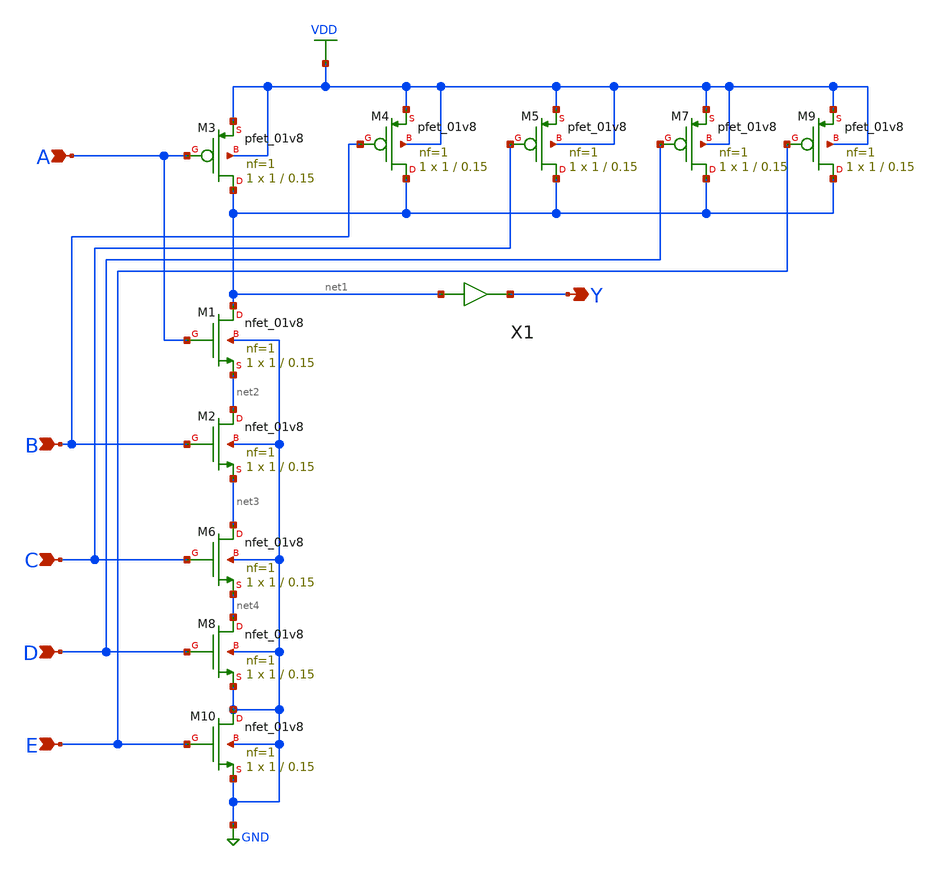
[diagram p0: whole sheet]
** sch_path: gates/AND5.sch
**.subckt AND5 A B Y C D E
*.ipin A
*.ipin B
*.opin Y
*.ipin C
*.ipin D
*.ipin E
XM1 net1 A net2 GND sky130_fd_pr__nfet_01v8 L=0.15 W=1 nf=1 ad='int((nf+1)/2) * W/nf * 0.29' as='int((nf+2)/2) * W/nf * 0.29'
+ pd='2*int((nf+1)/2) * (W/nf + 0.29)' ps='2*int((nf+2)/2) * (W/nf + 0.29)' nrd='0.29 / W' nrs='0.29 / W'
+ sa=0 sb=0 sd=0 mult=1 m=1
XM2 net2 B net3 GND sky130_fd_pr__nfet_01v8 L=0.15 W=1 nf=1 ad='int((nf+1)/2) * W/nf * 0.29' as='int((nf+2)/2) * W/nf * 0.29'
+ pd='2*int((nf+1)/2) * (W/nf + 0.29)' ps='2*int((nf+2)/2) * (W/nf + 0.29)' nrd='0.29 / W' nrs='0.29 / W'
+ sa=0 sb=0 sd=0 mult=1 m=1
XM3 net1 A VDD VDD sky130_fd_pr__pfet_01v8 L=0.15 W=1 nf=1 ad='int((nf+1)/2) * W/nf * 0.29' as='int((nf+2)/2) * W/nf * 0.29'
+ pd='2*int((nf+1)/2) * (W/nf + 0.29)' ps='2*int((nf+2)/2) * (W/nf + 0.29)' nrd='0.29 / W' nrs='0.29 / W'
+ sa=0 sb=0 sd=0 mult=1 m=1
XM4 net1 B VDD VDD sky130_fd_pr__pfet_01v8 L=0.15 W=1 nf=1 ad='int((nf+1)/2) * W/nf * 0.29' as='int((nf+2)/2) * W/nf * 0.29'
+ pd='2*int((nf+1)/2) * (W/nf + 0.29)' ps='2*int((nf+2)/2) * (W/nf + 0.29)' nrd='0.29 / W' nrs='0.29 / W'
+ sa=0 sb=0 sd=0 mult=1 m=1
XM5 net1 C VDD VDD sky130_fd_pr__pfet_01v8 L=0.15 W=1 nf=1 ad='int((nf+1)/2) * W/nf * 0.29' as='int((nf+2)/2) * W/nf * 0.29'
+ pd='2*int((nf+1)/2) * (W/nf + 0.29)' ps='2*int((nf+2)/2) * (W/nf + 0.29)' nrd='0.29 / W' nrs='0.29 / W'
+ sa=0 sb=0 sd=0 mult=1 m=1
XM6 net3 C net4 GND sky130_fd_pr__nfet_01v8 L=0.15 W=1 nf=1 ad='int((nf+1)/2) * W/nf * 0.29' as='int((nf+2)/2) * W/nf * 0.29'
+ pd='2*int((nf+1)/2) * (W/nf + 0.29)' ps='2*int((nf+2)/2) * (W/nf + 0.29)' nrd='0.29 / W' nrs='0.29 / W'
+ sa=0 sb=0 sd=0 mult=1 m=1
XM7 net1 D VDD VDD sky130_fd_pr__pfet_01v8 L=0.15 W=1 nf=1 ad='int((nf+1)/2) * W/nf * 0.29' as='int((nf+2)/2) * W/nf * 0.29'
+ pd='2*int((nf+1)/2) * (W/nf + 0.29)' ps='2*int((nf+2)/2) * (W/nf + 0.29)' nrd='0.29 / W' nrs='0.29 / W'
+ sa=0 sb=0 sd=0 mult=1 m=1
XM8 net4 D GND GND sky130_fd_pr__nfet_01v8 L=0.15 W=1 nf=1 ad='int((nf+1)/2) * W/nf * 0.29' as='int((nf+2)/2) * W/nf * 0.29'
+ pd='2*int((nf+1)/2) * (W/nf + 0.29)' ps='2*int((nf+2)/2) * (W/nf + 0.29)' nrd='0.29 / W' nrs='0.29 / W'
+ sa=0 sb=0 sd=0 mult=1 m=1
XM9 net1 E VDD VDD sky130_fd_pr__pfet_01v8 L=0.15 W=1 nf=1 ad='int((nf+1)/2) * W/nf * 0.29' as='int((nf+2)/2) * W/nf * 0.29'
+ pd='2*int((nf+1)/2) * (W/nf + 0.29)' ps='2*int((nf+2)/2) * (W/nf + 0.29)' nrd='0.29 / W' nrs='0.29 / W'
+ sa=0 sb=0 sd=0 mult=1 m=1
XM10 GND E GND GND sky130_fd_pr__nfet_01v8 L=0.15 W=1 nf=1 ad='int((nf+1)/2) * W/nf * 0.29' as='int((nf+2)/2) * W/nf * 0.29'
+ pd='2*int((nf+1)/2) * (W/nf + 0.29)' ps='2*int((nf+2)/2) * (W/nf + 0.29)' nrd='0.29 / W' nrs='0.29 / W'
+ sa=0 sb=0 sd=0 mult=1 m=1
X1 net1 Y inv_vtc
**.ends

* expanding   symbol:  /home/apn/test_xschem_sky130/inv_vtc.sym # of pins=2
** sym_path: gates/inv_vtc.sym
** sch_path: gates/inv_vtc.sch
.subckt inv_vtc A Y
*.ipin A
*.opin Y
XM1 Y A VDD VDD sky130_fd_pr__pfet_01v8 L=0.15 W=2 nf=1 ad='int((nf+1)/2) * W/nf * 0.29' as='int((nf+2)/2) * W/nf * 0.29'
+ pd='2*int((nf+1)/2) * (W/nf + 0.29)' ps='2*int((nf+2)/2) * (W/nf + 0.29)' nrd='0.29 / W' nrs='0.29 / W'
+ sa=0 sb=0 sd=0 mult=1 m=1
XM2 Y A GND GND sky130_fd_pr__nfet_01v8 L=0.15 W=1 nf=1 ad='int((nf+1)/2) * W/nf * 0.29' as='int((nf+2)/2) * W/nf * 0.29'
+ pd='2*int((nf+1)/2) * (W/nf + 0.29)' ps='2*int((nf+2)/2) * (W/nf + 0.29)' nrd='0.29 / W' nrs='0.29 / W'
+ sa=0 sb=0 sd=0 mult=1 m=1
.ends

.GLOBAL VDD
.GLOBAL GND
.end
